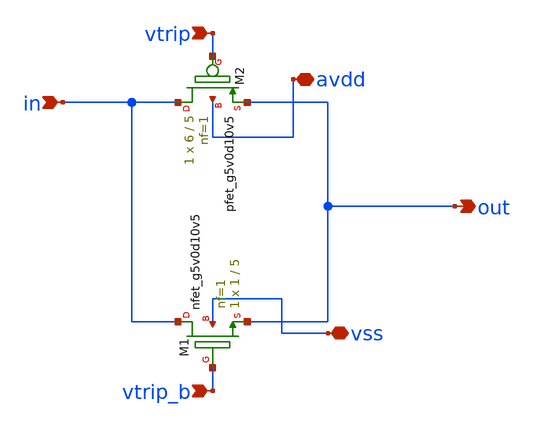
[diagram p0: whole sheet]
** sch_path: blocks/input/xschem/T_gate.sch
**.subckt T_gate avdd vss vtrip vtrip_b in out
*.iopin avdd
*.iopin vss
*.ipin vtrip
*.ipin vtrip_b
*.ipin in
*.opin out
XM1 in vtrip_b out vss sky130_fd_pr__nfet_g5v0d10v5 L=5 W=1 nf=1 ad='int((nf+1)/2) * W/nf * 0.29' as='int((nf+2)/2) * W/nf * 0.29'
+ pd='2*int((nf+1)/2) * (W/nf + 0.29)' ps='2*int((nf+2)/2) * (W/nf + 0.29)' nrd='0.29 / W' nrs='0.29 / W'
+ sa=0 sb=0 sd=0 mult=1 m=1
XM2 in vtrip out avdd sky130_fd_pr__pfet_g5v0d10v5 L=5 W=6 nf=1 ad='int((nf+1)/2) * W/nf * 0.29' as='int((nf+2)/2) * W/nf * 0.29'
+ pd='2*int((nf+1)/2) * (W/nf + 0.29)' ps='2*int((nf+2)/2) * (W/nf + 0.29)' nrd='0.29 / W' nrs='0.29 / W'
+ sa=0 sb=0 sd=0 mult=1 m=1
**.ends
.end
